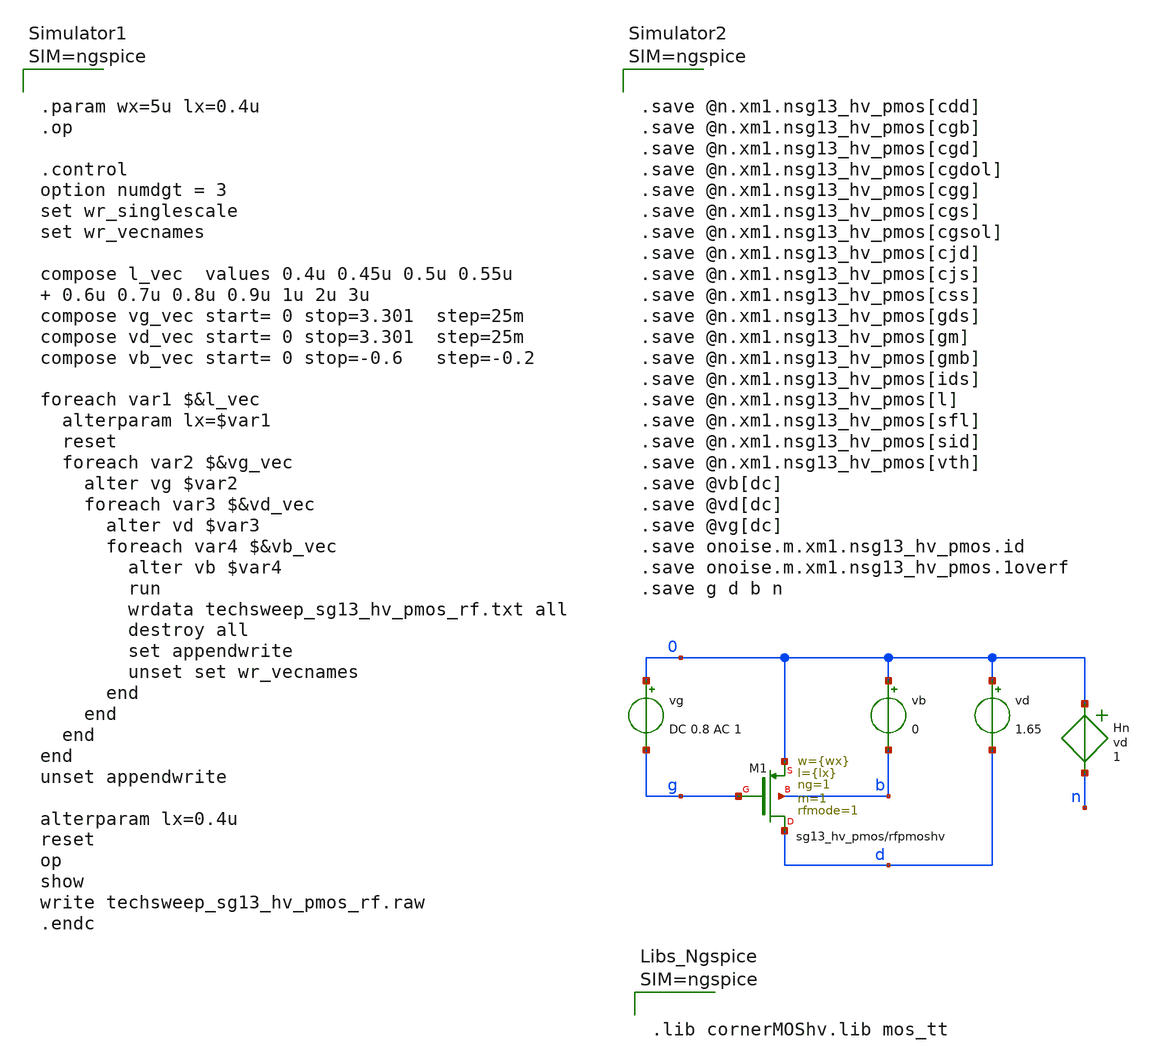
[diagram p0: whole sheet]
** sch_path: starter_files_open_source_tools/ihp-sg13cmos5l/techsweep_sg13_hv_pmos_rf.sch
**.subckt techsweep_sg13_hv_pmos_rf
Hn 0 n vd 1
vg 0 g DC 0.8 AC 1
vd 0 d 1.65
vb 0 b 0
XM1 d g 0 b sg13_hv_pmos w={wx} l={lx} ng=1 m=1 rfmode=1 mm_ok=1
**** begin user architecture code



.lib cornerMOShv.lib mos_tt






.save @n.xm1.nsg13_hv_pmos[cdd]
.save @n.xm1.nsg13_hv_pmos[cgb]
.save @n.xm1.nsg13_hv_pmos[cgd]
.save @n.xm1.nsg13_hv_pmos[cgdol]
.save @n.xm1.nsg13_hv_pmos[cgg]
.save @n.xm1.nsg13_hv_pmos[cgs]
.save @n.xm1.nsg13_hv_pmos[cgsol]
.save @n.xm1.nsg13_hv_pmos[cjd]
.save @n.xm1.nsg13_hv_pmos[cjs]
.save @n.xm1.nsg13_hv_pmos[css]
.save @n.xm1.nsg13_hv_pmos[gds]
.save @n.xm1.nsg13_hv_pmos[gm]
.save @n.xm1.nsg13_hv_pmos[gmb]
.save @n.xm1.nsg13_hv_pmos[ids]
.save @n.xm1.nsg13_hv_pmos[l]
.save @n.xm1.nsg13_hv_pmos[sfl]
.save @n.xm1.nsg13_hv_pmos[sid]
.save @n.xm1.nsg13_hv_pmos[vth]
.save @vb[dc]
.save @vd[dc]
.save @vg[dc]
.save onoise.m.xm1.nsg13_hv_pmos.id
.save onoise.m.xm1.nsg13_hv_pmos.1overf
.save g d b n






.param wx=5u lx=0.4u
.op

.control
option numdgt = 3
set wr_singlescale
set wr_vecnames

compose l_vec  values 0.4u 0.45u 0.5u 0.55u  0.6u 0.7u 0.8u 0.9u 1u 2u 3u
compose vg_vec start= 0 stop=3.301  step=25m
compose vd_vec start= 0 stop=3.301  step=25m
compose vb_vec start= 0 stop=-0.6   step=-0.2

foreach var1 $&l_vec
  alterparam lx=$var1
  reset
  foreach var2 $&vg_vec
    alter vg $var2
    foreach var3 $&vd_vec
      alter vd $var3
      foreach var4 $&vb_vec
        alter vb $var4
        run
        wrdata techsweep_sg13_hv_pmos_rf.txt all
        destroy all
        set appendwrite
        unset set wr_vecnames
      end
    end
  end
end
unset appendwrite

alterparam lx=0.4u
reset
op
show
write techsweep_sg13_hv_pmos_rf.raw
.endc



**** end user architecture code
**.ends
.end
